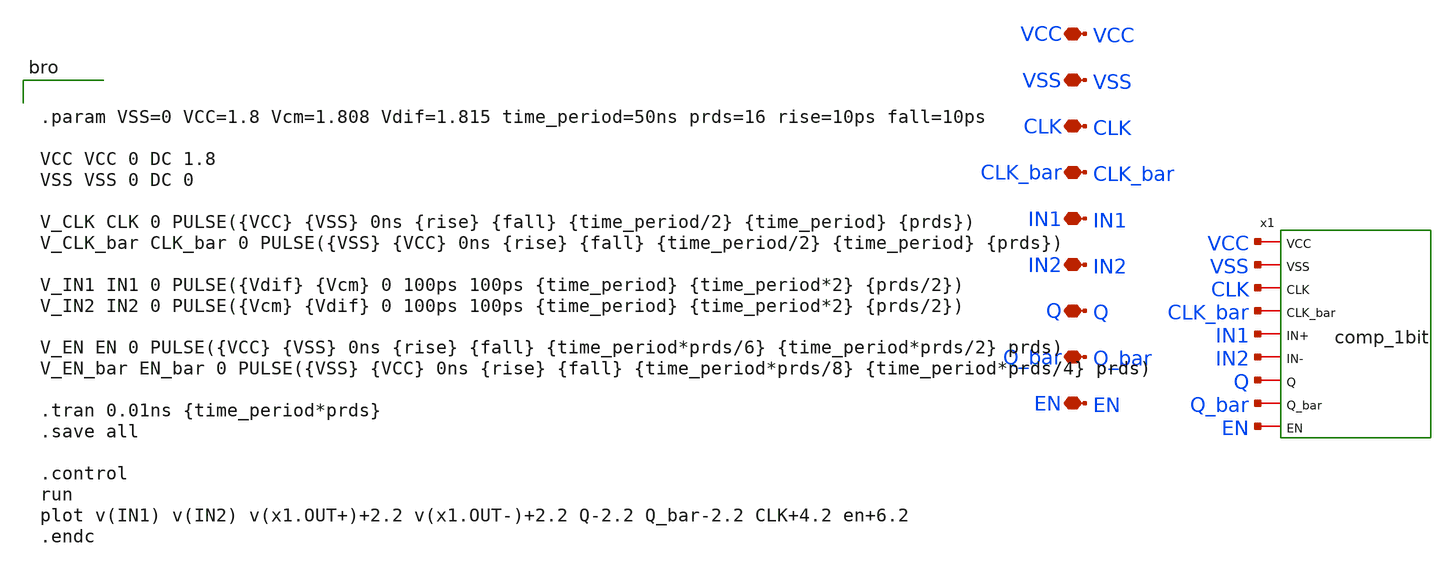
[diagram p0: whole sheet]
** sch_path: voltage_comp/comp_1bit_test.sch
**.subckt comp_1bit_test VSS VCC IN1 IN2 CLK CLK_bar Q Q_bar EN
*.iopin VSS
*.iopin VCC
*.iopin IN1
*.iopin IN2
*.iopin CLK
*.iopin CLK_bar
*.iopin Q
*.iopin Q_bar
*.iopin EN
x1 VCC VSS CLK CLK_bar IN1 IN2 Q Q_bar EN comp_1bit
**** begin user architecture code


.param VSS=0 VCC=1.8 Vcm=1.808 Vdif=1.815 time_period=50ns prds=16 rise=10ps fall=10ps

VCC VCC 0 DC 1.8
VSS VSS 0 DC 0

V_CLK CLK 0 PULSE({VCC} {VSS} 0ns {rise} {fall} {time_period/2} {time_period} {prds})
V_CLK_bar CLK_bar 0 PULSE({VSS} {VCC} 0ns {rise} {fall} {time_period/2} {time_period} {prds})

V_IN1 IN1 0 PULSE({Vdif} {Vcm} 0 100ps 100ps {time_period} {time_period*2} {prds/2})
V_IN2 IN2 0 PULSE({Vcm} {Vdif} 0 100ps 100ps {time_period} {time_period*2} {prds/2})

V_EN EN 0 PULSE({VCC} {VSS} 0ns {rise} {fall} {time_period*prds/6} {time_period*prds/2} prds)
V_EN_bar EN_bar 0 PULSE({VSS} {VCC} 0ns {rise} {fall} {time_period*prds/8} {time_period*prds/4} prds)

.tran 0.01ns {time_period*prds}
.save all

.control
run
plot v(IN1) v(IN2) v(x1.OUT+)+2.2 v(x1.OUT-)+2.2 Q-2.2 Q_bar-2.2 CLK+4.2 en+6.2
.endc



** opencircuitdesign pdks install
.lib $::SKYWATER_MODELS/sky130.lib.spice tt

**** end user architecture code
**.ends
.end
